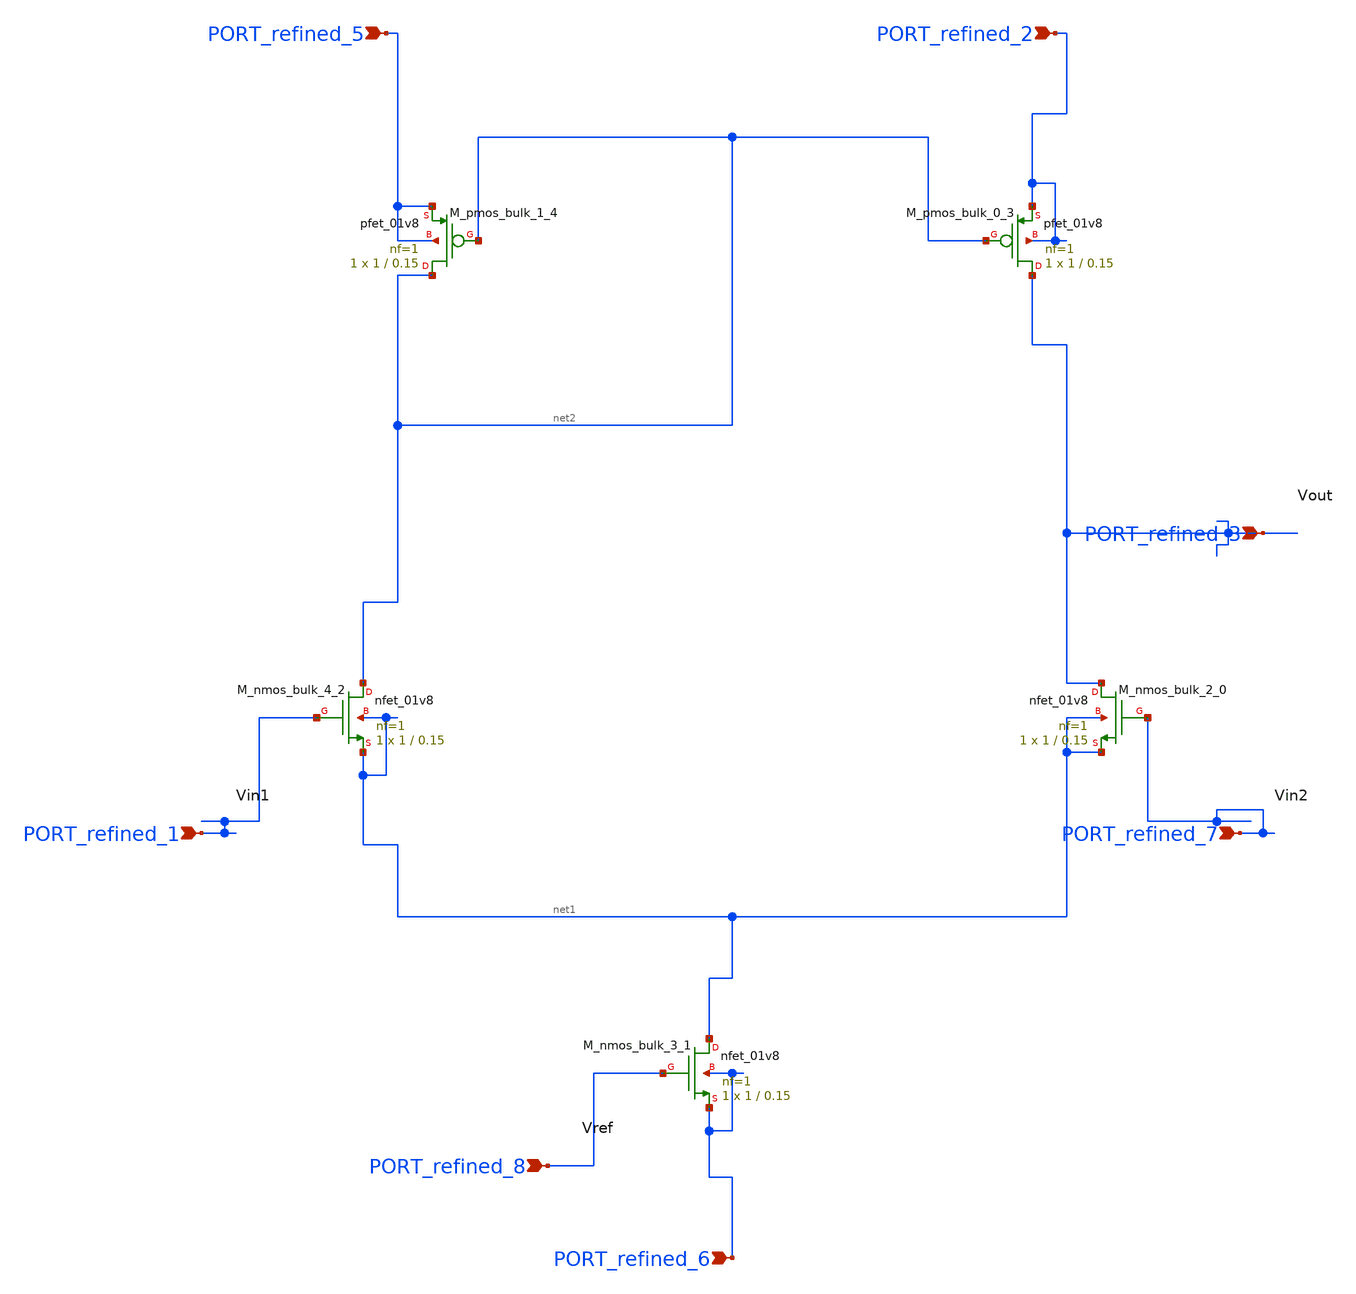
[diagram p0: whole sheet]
** sch_path: schematics/10_1007_s42452-023-05572-9_09_002.sch
**.subckt 10_1007_s42452-023-05572-9_09_002 PORT_refined_8 PORT_refined_3 PORT_refined_2
*+ PORT_refined_5 PORT_refined_6 PORT_refined_1 PORT_refined_7
*.ipin PORT_refined_8
*.ipin PORT_refined_3
*.ipin PORT_refined_2
*.ipin PORT_refined_5
*.ipin PORT_refined_6
*.ipin PORT_refined_1
*.ipin PORT_refined_7
XM_nmos_bulk_2_0 PORT_refined_3 PORT_refined_7 net1 net1 sky130_fd_pr__nfet_01v8 L=0.15 W=1 nf=1 ad='int((1 + 1)/2) * 1 / 1 * 0.29'
+ as='int((1 + 2)/2) * 1 / 1 * 0.29' pd='2*int((1 + 1)/2) * (1 / 1 + 0.29)' ps='2*int((1 + 2)/2) * (1 / 1 + 0.29)'
+ nrd='0.29 / 1 ' nrs='0.29 / 1 ' sa=0 sb=0 sd=0 mult=1 m=1
XM_nmos_bulk_3_1 net1 PORT_refined_8 PORT_refined_6 PORT_refined_6 sky130_fd_pr__nfet_01v8 L=0.15 W=1
+ nf=1 ad='int((1 + 1)/2) * 1 / 1 * 0.29' as='int((1 + 2)/2) * 1 / 1 * 0.29' pd='2*int((1 + 1)/2) * (1 / 1 + 0.29)'
+ ps='2*int((1 + 2)/2) * (1 / 1 + 0.29)' nrd='0.29 / 1 ' nrs='0.29 / 1 ' sa=0 sb=0 sd=0 mult=1 m=1
XM_nmos_bulk_4_2 net2 PORT_refined_1 net1 net1 sky130_fd_pr__nfet_01v8 L=0.15 W=1 nf=1 ad='int((1 + 1)/2) * 1 / 1 * 0.29'
+ as='int((1 + 2)/2) * 1 / 1 * 0.29' pd='2*int((1 + 1)/2) * (1 / 1 + 0.29)' ps='2*int((1 + 2)/2) * (1 / 1 + 0.29)'
+ nrd='0.29 / 1 ' nrs='0.29 / 1 ' sa=0 sb=0 sd=0 mult=1 m=1
XM_pmos_bulk_0_3 PORT_refined_3 net2 PORT_refined_2 PORT_refined_2 sky130_fd_pr__pfet_01v8 L=0.15 W=1
+ nf=1 ad='int((1 + 1)/2) * 1 / 1 * 0.29' as='int((1 + 2)/2) * 1 / 1 * 0.29' pd='2*int((1 + 1)/2) * (1 / 1 + 0.29)'
+ ps='2*int((1 + 2)/2) * (1 / 1 + 0.29)' nrd='0.29 / 1 ' nrs='0.29 / 1 ' sa=0 sb=0 sd=0 mult=1 m=1
XM_pmos_bulk_1_4 net2 net2 PORT_refined_5 PORT_refined_5 sky130_fd_pr__pfet_01v8 L=0.15 W=1 nf=1 ad='int((1 + 1)/2) * 1 / 1 * 0.29'
+ as='int((1 + 2)/2) * 1 / 1 * 0.29' pd='2*int((1 + 1)/2) * (1 / 1 + 0.29)' ps='2*int((1 + 2)/2) * (1 / 1 + 0.29)'
+ nrd='0.29 / 1 ' nrs='0.29 / 1 ' sa=0 sb=0 sd=0 mult=1 m=1
**.ends
.end
